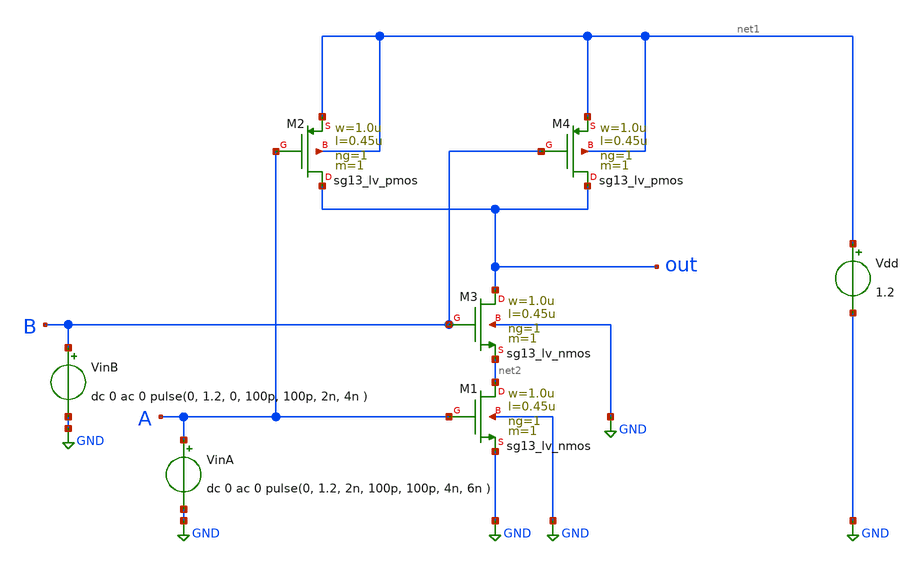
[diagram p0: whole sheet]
** sch_path: ihp-sg13g2/xschem_libs/sg13g2_tests_ase/tran_logic_nand/schematic/tran_logic_nand.sch
* Copyright 2023 IHP PDK Authors
**.subckt tran_logic_nand
VinA A GND dc 0 ac 0 pulse(0, 1.2, 2n, 100p, 100p, 4n, 6n )
Vdd net1 GND 1.2
VinB B GND dc 0 ac 0 pulse(0, 1.2, 0, 100p, 100p, 2n, 4n )
XM1 net2 A GND GND sg13_lv_nmos w=1.0u l=0.45u ng=1 m=1 mm_ok=1
XM3 out B net2 GND sg13_lv_nmos w=1.0u l=0.45u ng=1 m=1 mm_ok=1
XM2 out A net1 net1 sg13_lv_pmos w=1.0u l=0.45u ng=1 m=1 mm_ok=1
XM4 out B net1 net1 sg13_lv_pmos w=1.0u l=0.45u ng=1 m=1 mm_ok=1
**.ends
.GLOBAL GND
.end
